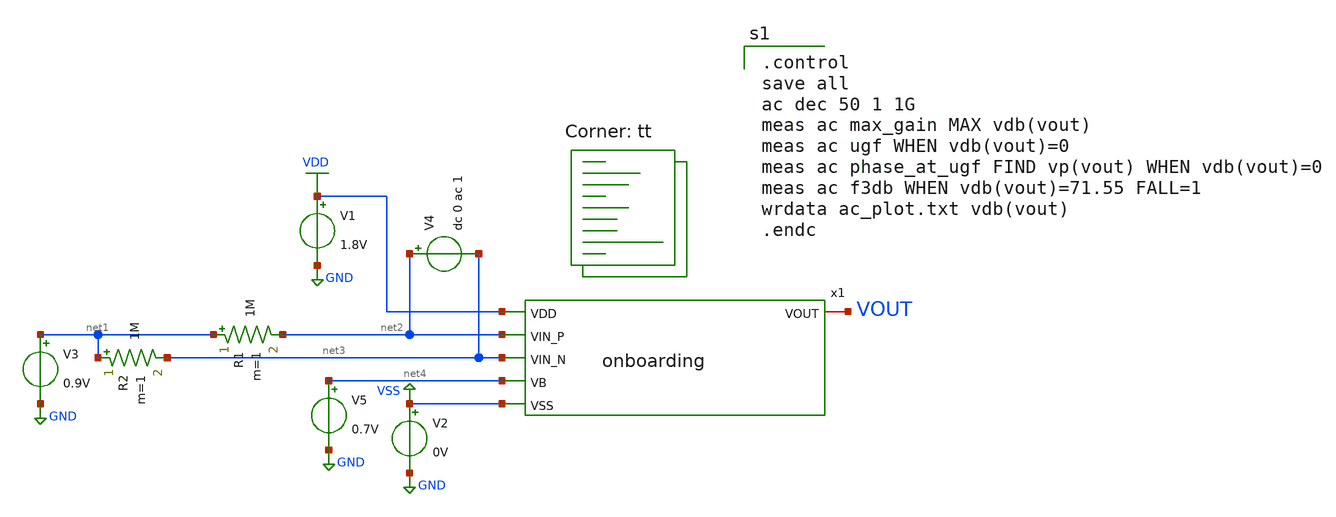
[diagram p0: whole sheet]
** sch_path: analog/bootcamp_opamp/build/schematic/tb_ac_analysis.sch
**.subckt tb_ac_analysis
V1 VDD GND 1.8V
V2 VSS GND 0V
V3 net1 GND 0.9V
V4 net2 net3 dc 0 ac 1
R1 net1 net2 1M m=1
R2 net1 net3 1M m=1
V5 net4 GND 0.7V
x1 VDD VOUT net2 net3 net4 VSS onboarding
**** begin user architecture code
.lib $::SKYWATER_MODELS/sky130.lib.spice tt

.control
save all
ac dec 50 1 1G
meas ac max_gain MAX vdb(vout)
meas ac ugf WHEN vdb(vout)=0
meas ac phase_at_ugf FIND vp(vout) WHEN vdb(vout)=0
meas ac f3db WHEN vdb(vout)=71.55 FALL=1
wrdata ac_plot.txt vdb(vout)
.endc

**** end user architecture code
**.ends

* expanding   symbol:  onboarding.sym # of pins=6
** sym_path: analog/bootcamp_opamp/build/schematic/onboarding.sym
** sch_path: analog/bootcamp_opamp/build/schematic/onboarding.sch
.subckt onboarding VDD VOUT VIN_P VIN_N VB VSS
*.ipin VIN_P
*.ipin VDD
*.ipin VSS
*.ipin VB
*.ipin VIN_N
*.iopin VOUT
XC1 net4 VOUT sky130_fd_pr__cap_mim_m3_1 W=45 L=45 MF=1 m=1
XM6 VOUT net1 VDD VDD sky130_fd_pr__pfet_01v8 L=0.5 W=6 nf=1 ad='int((nf+1)/2) * W/nf * 0.29' as='int((nf+2)/2) * W/nf * 0.29'
+ pd='2*int((nf+1)/2) * (W/nf + 0.29)' ps='2*int((nf+2)/2) * (W/nf + 0.29)' nrd='0.29 / W' nrs='0.29 / W'
+ sa=0 sb=0 sd=0 mult=60 m=60
XM1 net3 VIN_P net2 VSS sky130_fd_pr__nfet_01v8 L=0.5 W=2 nf=1 ad='int((nf+1)/2) * W/nf * 0.29' as='int((nf+2)/2) * W/nf * 0.29'
+ pd='2*int((nf+1)/2) * (W/nf + 0.29)' ps='2*int((nf+2)/2) * (W/nf + 0.29)' nrd='0.29 / W' nrs='0.29 / W'
+ sa=0 sb=0 sd=0 mult=1 m=1
XM2 net1 VIN_N net2 VSS sky130_fd_pr__nfet_01v8 L=0.5 W=2 nf=1 ad='int((nf+1)/2) * W/nf * 0.29' as='int((nf+2)/2) * W/nf * 0.29'
+ pd='2*int((nf+1)/2) * (W/nf + 0.29)' ps='2*int((nf+2)/2) * (W/nf + 0.29)' nrd='0.29 / W' nrs='0.29 / W'
+ sa=0 sb=0 sd=0 mult=1 m=1
XM4 net1 net3 VDD VDD sky130_fd_pr__pfet_01v8 L=0.5 W=6 nf=1 ad='int((nf+1)/2) * W/nf * 0.29' as='int((nf+2)/2) * W/nf * 0.29'
+ pd='2*int((nf+1)/2) * (W/nf + 0.29)' ps='2*int((nf+2)/2) * (W/nf + 0.29)' nrd='0.29 / W' nrs='0.29 / W'
+ sa=0 sb=0 sd=0 mult=1 m=1
XM3 net3 net3 VDD VDD sky130_fd_pr__pfet_01v8 L=0.5 W=6 nf=1 ad='int((nf+1)/2) * W/nf * 0.29' as='int((nf+2)/2) * W/nf * 0.29'
+ pd='2*int((nf+1)/2) * (W/nf + 0.29)' ps='2*int((nf+2)/2) * (W/nf + 0.29)' nrd='0.29 / W' nrs='0.29 / W'
+ sa=0 sb=0 sd=0 mult=1 m=1
XM5 net2 VB VSS VSS sky130_fd_pr__nfet_01v8 L=0.5 W=2 nf=1 ad='int((nf+1)/2) * W/nf * 0.29' as='int((nf+2)/2) * W/nf * 0.29'
+ pd='2*int((nf+1)/2) * (W/nf + 0.29)' ps='2*int((nf+2)/2) * (W/nf + 0.29)' nrd='0.29 / W' nrs='0.29 / W'
+ sa=0 sb=0 sd=0 mult=1 m=1
XM7 VOUT VB VSS VSS sky130_fd_pr__nfet_01v8 L=0.5 W=4.6 nf=1 ad='int((nf+1)/2) * W/nf * 0.29' as='int((nf+2)/2) * W/nf * 0.29'
+ pd='2*int((nf+1)/2) * (W/nf + 0.29)' ps='2*int((nf+2)/2) * (W/nf + 0.29)' nrd='0.29 / W' nrs='0.29 / W'
+ sa=0 sb=0 sd=0 mult=10 m=10
XR1 net4 net1 sky130_fd_pr__res_generic_po W=1 L=5 m=1
.ends

.GLOBAL VDD
.GLOBAL GND
.GLOBAL VSS
.end
